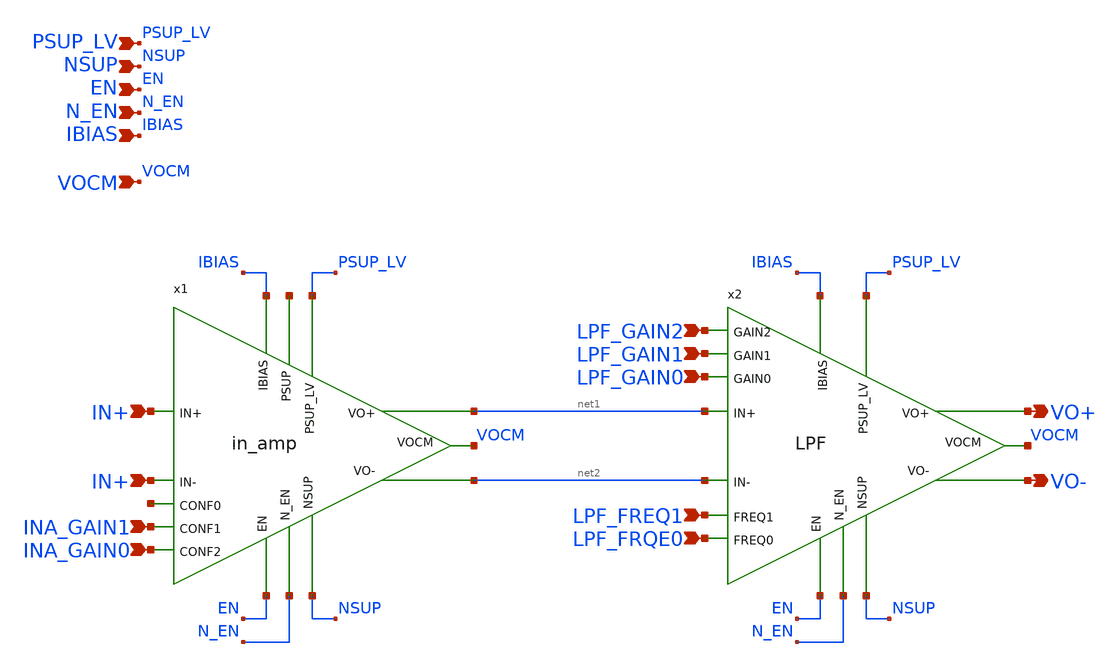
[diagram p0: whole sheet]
** sch_path: xschem/top.sch
**.subckt top IN+ IN+ EN N_EN NSUP PSUP_LV IBIAS VOCM VO+ VO- LPF_GAIN2 LPF_GAIN1 LPF_GAIN0
*+ LPF_FREQ1 LPF_FRQE0 INA_GAIN1 INA_GAIN0
*.ipin IN+
*.ipin IN+
*.ipin EN
*.ipin N_EN
*.ipin NSUP
*.ipin PSUP_LV
*.ipin IBIAS
*.ipin VOCM
*.opin VO+
*.opin VO-
*.ipin LPF_GAIN2
*.ipin LPF_GAIN1
*.ipin LPF_GAIN0
*.ipin LPF_FREQ1
*.ipin LPF_FRQE0
*.ipin INA_GAIN1
*.ipin INA_GAIN0
x1 net3 PSUP_LV NSUP EN N_EN IBIAS net4 INA_GAIN1 INA_GAIN0 IN+ net1 VOCM IN+ net2 in_amp
x2 PSUP_LV NSUP EN N_EN IBIAS LPF_GAIN2 LPF_GAIN1 LPF_GAIN0 LPF_FREQ1 LPF_FRQE0 net1 VO+ VOCM net2
+ VO- LPF
**.ends
.end
